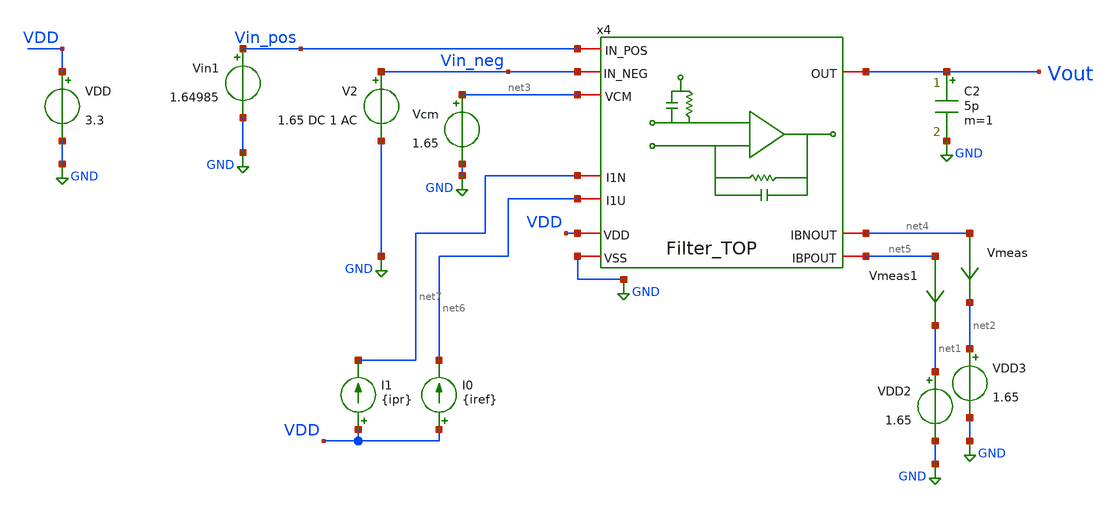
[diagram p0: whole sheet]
** sch_path: TIA_Filter/untitled.sch
**.subckt untitled
VDD VDD GND 3.3
C2 Vout GND 5p m=1
Vin1 Vin_pos GND 1.64985
V2 Vin_neg GND 1.65 DC 1 AC
I0 VDD net6 {iref}
I1 VDD net7 {ipr}
Vmeas net4 net2 0
.save i(vmeas)
Vmeas1 net5 net1 0
.save i(vmeas1)
Vcm net3 GND 1.65
VDD2 net1 GND 1.65
VDD3 net2 GND 1.65
x4 Vin_pos Vin_neg net3 Vout VDD GND net7 net6 net4 net5 Filter_TOP
**.ends
.GLOBAL GND
.end
